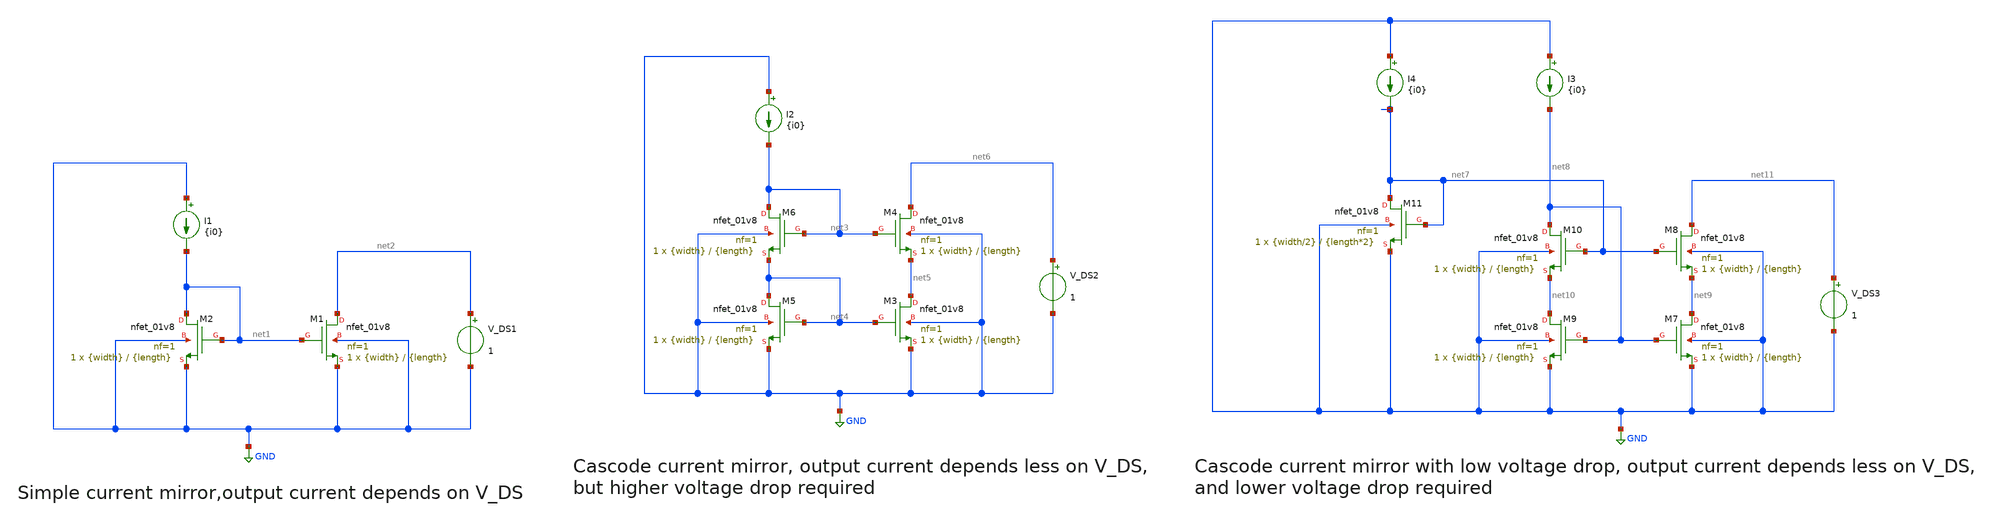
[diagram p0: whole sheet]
** sch_path: xschem/current_mirrors.sch
**.subckt current_mirrors
XM1 net2 net1 GND GND sky130_fd_pr__nfet_01v8 L={length} W={width} nf=1 ad='int((nf+1)/2) * W/nf * 0.29'
+ as='int((nf+2)/2) * W/nf * 0.29' pd='2*int((nf+1)/2) * (W/nf + 0.29)' ps='2*int((nf+2)/2) * (W/nf + 0.29)'
+ nrd='0.29 / W' nrs='0.29 / W' sa=0 sb=0 sd=0 mult=1 m=1
XM2 net1 net1 GND GND sky130_fd_pr__nfet_01v8 L={length} W={width} nf=1 ad='int((nf+1)/2) * W/nf * 0.29'
+ as='int((nf+2)/2) * W/nf * 0.29' pd='2*int((nf+1)/2) * (W/nf + 0.29)' ps='2*int((nf+2)/2) * (W/nf + 0.29)'
+ nrd='0.29 / W' nrs='0.29 / W' sa=0 sb=0 sd=0 mult=1 m=1
V_DS1 net2 GND 1
I1 GND net1 {i0}
XM3 net5 net4 GND GND sky130_fd_pr__nfet_01v8 L={length} W={width} nf=1 ad='int((nf+1)/2) * W/nf * 0.29'
+ as='int((nf+2)/2) * W/nf * 0.29' pd='2*int((nf+1)/2) * (W/nf + 0.29)' ps='2*int((nf+2)/2) * (W/nf + 0.29)'
+ nrd='0.29 / W' nrs='0.29 / W' sa=0 sb=0 sd=0 mult=1 m=1
XM4 net6 net3 net5 GND sky130_fd_pr__nfet_01v8 L={length} W={width} nf=1 ad='int((nf+1)/2) * W/nf * 0.29'
+ as='int((nf+2)/2) * W/nf * 0.29' pd='2*int((nf+1)/2) * (W/nf + 0.29)' ps='2*int((nf+2)/2) * (W/nf + 0.29)'
+ nrd='0.29 / W' nrs='0.29 / W' sa=0 sb=0 sd=0 mult=1 m=1
XM5 net4 net4 GND GND sky130_fd_pr__nfet_01v8 L={length} W={width} nf=1 ad='int((nf+1)/2) * W/nf * 0.29'
+ as='int((nf+2)/2) * W/nf * 0.29' pd='2*int((nf+1)/2) * (W/nf + 0.29)' ps='2*int((nf+2)/2) * (W/nf + 0.29)'
+ nrd='0.29 / W' nrs='0.29 / W' sa=0 sb=0 sd=0 mult=1 m=1
XM6 net3 net3 net4 GND sky130_fd_pr__nfet_01v8 L={length} W={width} nf=1 ad='int((nf+1)/2) * W/nf * 0.29'
+ as='int((nf+2)/2) * W/nf * 0.29' pd='2*int((nf+1)/2) * (W/nf + 0.29)' ps='2*int((nf+2)/2) * (W/nf + 0.29)'
+ nrd='0.29 / W' nrs='0.29 / W' sa=0 sb=0 sd=0 mult=1 m=1
I2 GND net3 {i0}
V_DS2 net6 GND 1
XM7 net9 net8 GND GND sky130_fd_pr__nfet_01v8 L={length} W={width} nf=1 ad='int((nf+1)/2) * W/nf * 0.29'
+ as='int((nf+2)/2) * W/nf * 0.29' pd='2*int((nf+1)/2) * (W/nf + 0.29)' ps='2*int((nf+2)/2) * (W/nf + 0.29)'
+ nrd='0.29 / W' nrs='0.29 / W' sa=0 sb=0 sd=0 mult=1 m=1
XM8 net11 net7 net9 GND sky130_fd_pr__nfet_01v8 L={length} W={width} nf=1 ad='int((nf+1)/2) * W/nf * 0.29'
+ as='int((nf+2)/2) * W/nf * 0.29' pd='2*int((nf+1)/2) * (W/nf + 0.29)' ps='2*int((nf+2)/2) * (W/nf + 0.29)'
+ nrd='0.29 / W' nrs='0.29 / W' sa=0 sb=0 sd=0 mult=1 m=1
XM9 net10 net8 GND GND sky130_fd_pr__nfet_01v8 L={length} W={width} nf=1 ad='int((nf+1)/2) * W/nf * 0.29'
+ as='int((nf+2)/2) * W/nf * 0.29' pd='2*int((nf+1)/2) * (W/nf + 0.29)' ps='2*int((nf+2)/2) * (W/nf + 0.29)'
+ nrd='0.29 / W' nrs='0.29 / W' sa=0 sb=0 sd=0 mult=1 m=1
XM10 net8 net7 net10 GND sky130_fd_pr__nfet_01v8 L={length} W={width} nf=1 ad='int((nf+1)/2) * W/nf * 0.29'
+ as='int((nf+2)/2) * W/nf * 0.29' pd='2*int((nf+1)/2) * (W/nf + 0.29)' ps='2*int((nf+2)/2) * (W/nf + 0.29)'
+ nrd='0.29 / W' nrs='0.29 / W' sa=0 sb=0 sd=0 mult=1 m=1
I3 GND net8 {i0}
V_DS3 net11 GND 1
XM11 net7 net7 GND GND sky130_fd_pr__nfet_01v8 L={length*2} W={width/2} nf=1 ad='int((nf+1)/2) * W/nf * 0.29'
+ as='int((nf+2)/2) * W/nf * 0.29' pd='2*int((nf+1)/2) * (W/nf + 0.29)' ps='2*int((nf+2)/2) * (W/nf + 0.29)'
+ nrd='0.29 / W' nrs='0.29 / W' sa=0 sb=0 sd=0 mult=1 m=1
I4 GND net7 {i0}
**** begin user architecture code

.lib /opt/pdks/sky130A/libs.tech/ngspice/sky130.lib.spice tt


.control
save all
dc V_DS1 0 1.8 0.025
plot -i(V_DS1)
dc V_DS2 0 1.8 0.025
plot -i(V_DS2)
dc V_DS3 0 1.8 0.025
plot -i(V_DS3)
.endc



.param i0=1m
.param width=30
.param length=2


**** end user architecture code
**.ends
.GLOBAL GND
.end
